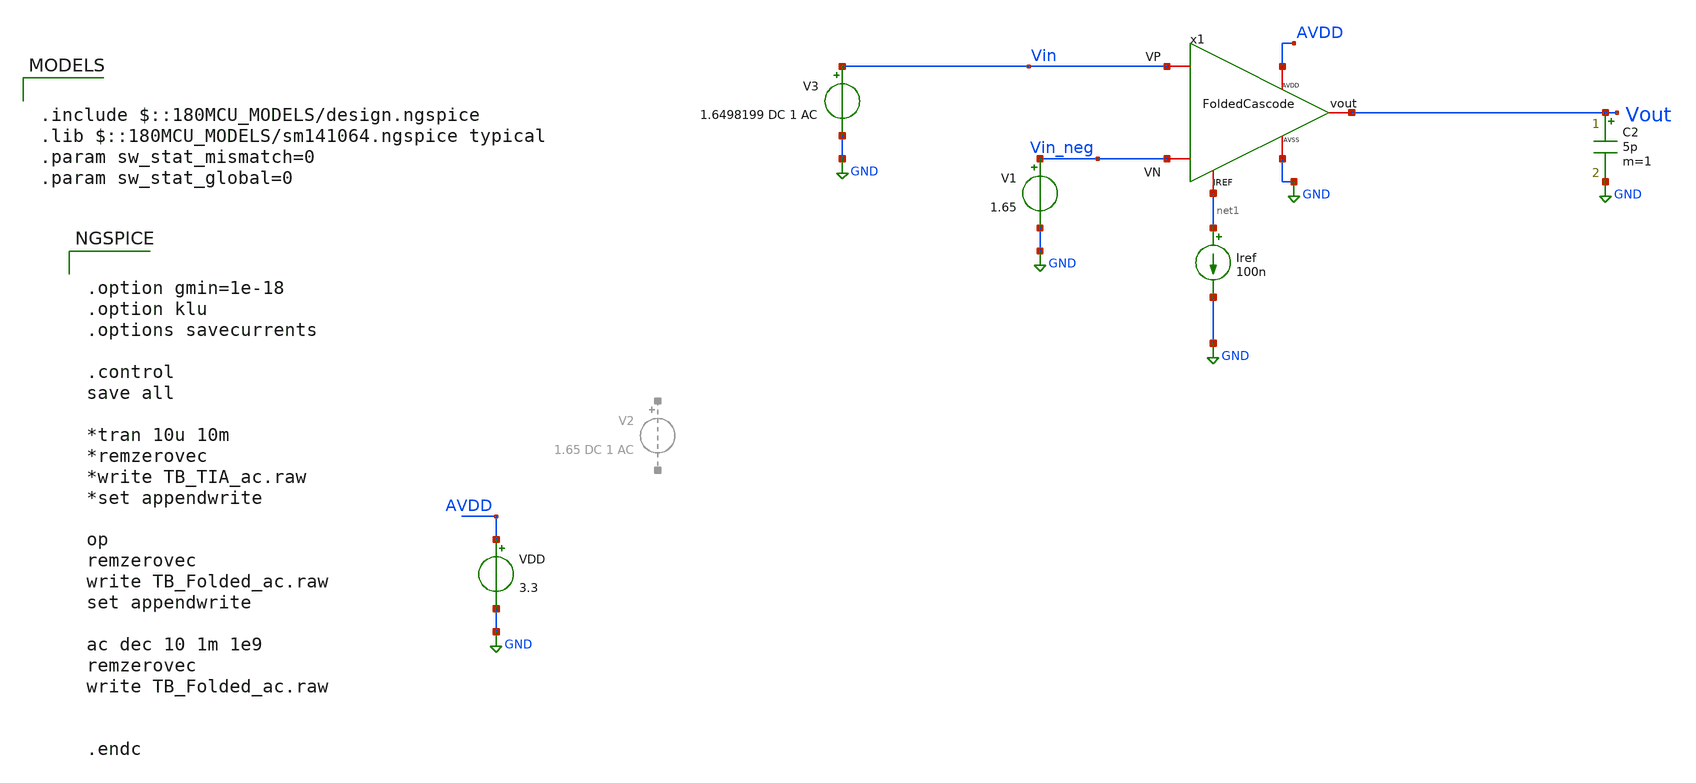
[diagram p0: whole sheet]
** sch_path: TIA_Filter/Folded/TB_Folded_ac.sch
**.subckt TB_Folded_ac
VDD AVDD GND 3.3
Iref net1 GND 100n
V1 Vin_neg GND 1.65
C2 Vout GND 5p m=1
x1 Vin Vin_neg Vout net1 AVDD GND FoldedCascode
V3 Vin GND 1.6498199 DC 1 AC
**** begin user architecture code

.include $::180MCU_MODELS/design.ngspice
.lib $::180MCU_MODELS/sm141064.ngspice typical
.param sw_stat_mismatch=0
.param sw_stat_global=0



.option gmin=1e-18
.option klu
.options savecurrents

.control
save all

*tran 10u 10m
*remzerovec
*write TB_TIA_ac.raw
*set appendwrite

op
remzerovec
write TB_Folded_ac.raw
set appendwrite

ac dec 10 1m 1e9
remzerovec
write TB_Folded_ac.raw


.endc


**** end user architecture code
**.ends
.GLOBAL GND
.end
